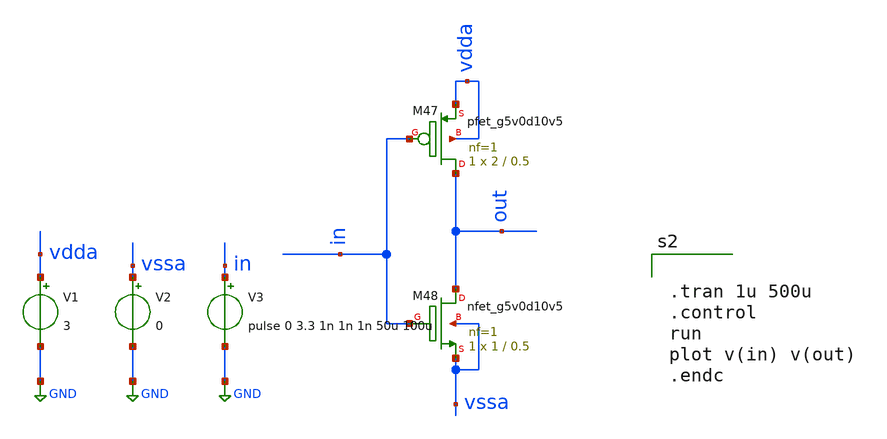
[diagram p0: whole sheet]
** sch_path: xschem/FDC/inverter1.sch
**.subckt inverter1
XM47 out in vdda vdda sky130_fd_pr__pfet_g5v0d10v5 L=0.5 W=2 nf=1 ad='int((nf+1)/2) * W/nf * 0.29' as='int((nf+2)/2) * W/nf * 0.29'
+ pd='2*int((nf+1)/2) * (W/nf + 0.29)' ps='2*int((nf+2)/2) * (W/nf + 0.29)' nrd='0.29 / W' nrs='0.29 / W'
+ sa=0 sb=0 sd=0 mult=1 m=1
XM48 out in vssa vssa sky130_fd_pr__nfet_g5v0d10v5 L=0.5 W=1 nf=1 ad='int((nf+1)/2) * W/nf * 0.29' as='int((nf+2)/2) * W/nf * 0.29'
+ pd='2*int((nf+1)/2) * (W/nf + 0.29)' ps='2*int((nf+2)/2) * (W/nf + 0.29)' nrd='0.29 / W' nrs='0.29 / W'
+ sa=0 sb=0 sd=0 mult=1 m=1
V1 vdda GND 3
V2 vssa GND 0
V3 in GND pulse 0 3.3 1n 1n 1n 50u 100u
**** begin user architecture code

.lib ~/open_pdks/sky130/sky130A/libs.tech/ngspice/sky130.lib.spice tt
*.MODEL swmod SW(VT=0.0 VH=0.01 RON=1 ROFF=10000000000)
.param mc_mm_switch=0
.param mc_pr_switch=0


.tran 1u 500u
.control
run
plot v(in) v(out)
.endc

**** end user architecture code
**.ends
.GLOBAL GND
.end
